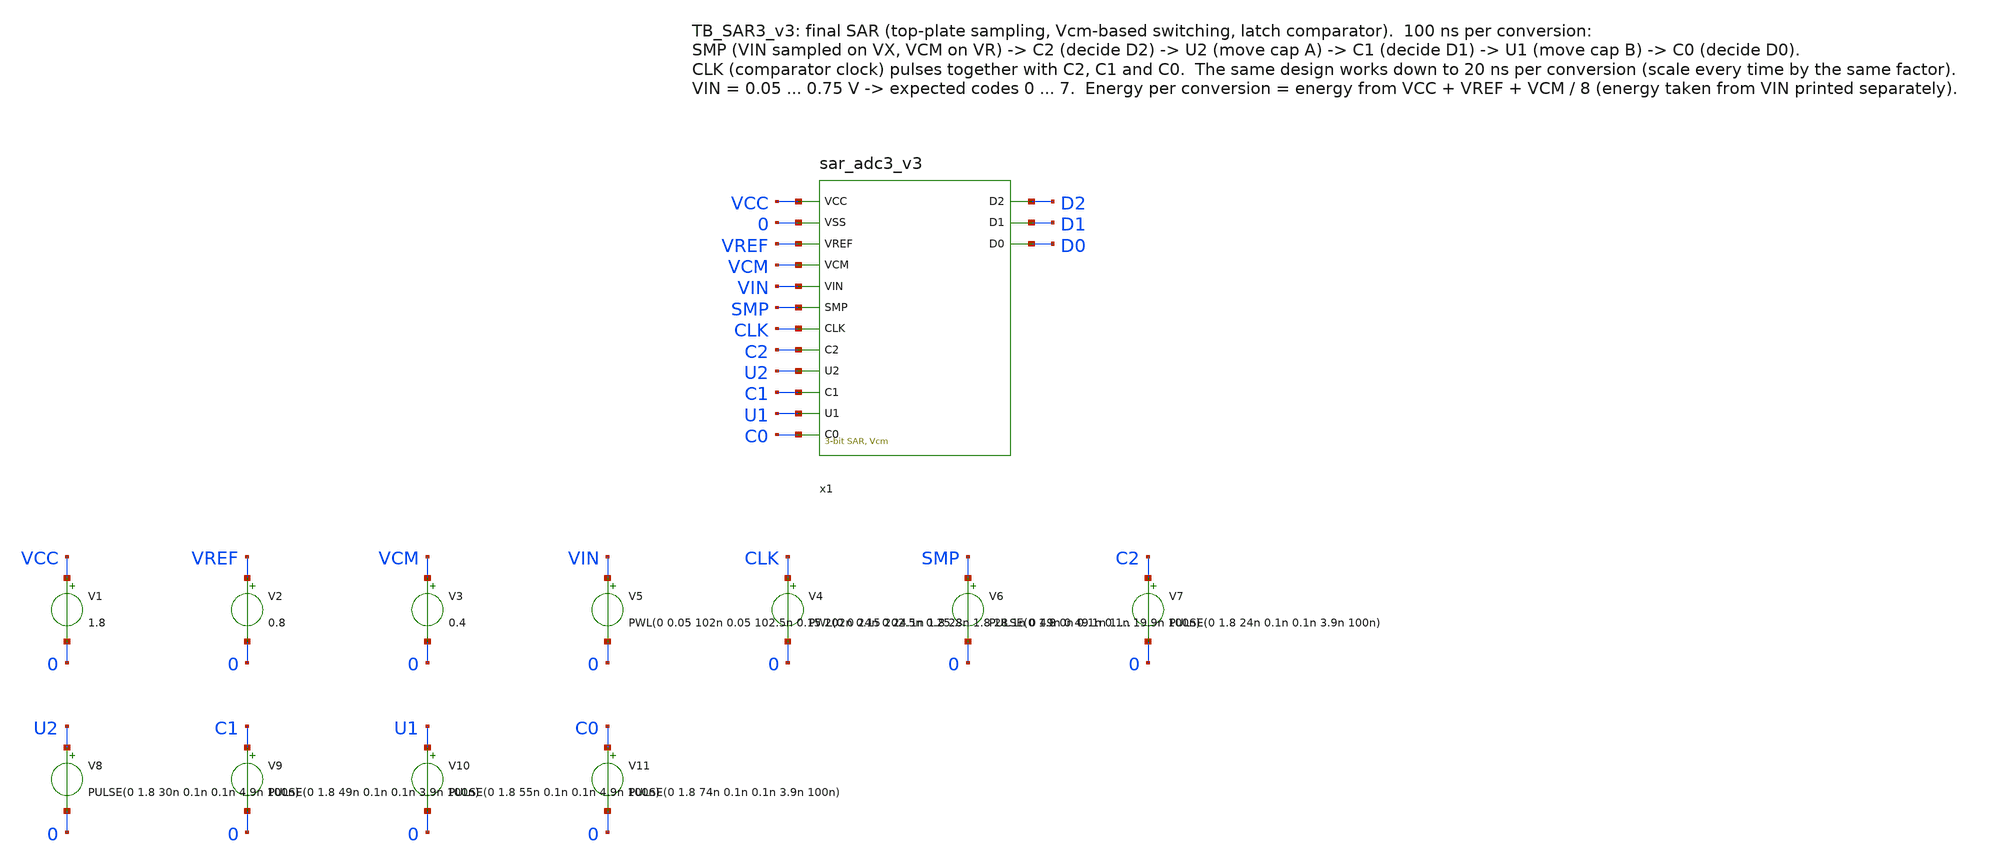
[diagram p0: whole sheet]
** sch_path: SAR_improved/TB_SAR3_v3.sch
**.subckt TB_SAR3_v3
x1 VCC 0 VREF VCM VIN SMP CLK C2 U2 C1 U1 C0 D2 D1 D0 sar_adc3_v3
V1 VCC 0 1.8
V2 VREF 0 0.8
V3 VCM 0 0.4
V5 VIN 0 PWL(0 0.05 102n 0.05 102.5n 0.15 202n 0.15 202.5n 0.25 302n 0.25 302.5n 0.35 402n 0.35
+ 402.5n 0.45 502n 0.45 502.5n 0.55 602n 0.55 602.5n 0.65 702n 0.65 702.5n 0.75)
V4 CLK 0 PWL(0 0 24n 0 24.1n 1.8 28n 1.8 28.1n 0 49n 0 49.1n 1.8 53n 1.8 53.1n 0 74n 0 74.1n 1.8 78n
+ 1.8 78.1n 0 100n 0) r=0
V6 SMP 0 PULSE(0 1.8 0n 0.1n 0.1n 19.9n 100n)
V7 C2 0 PULSE(0 1.8 24n 0.1n 0.1n 3.9n 100n)
V8 U2 0 PULSE(0 1.8 30n 0.1n 0.1n 4.9n 100n)
V9 C1 0 PULSE(0 1.8 49n 0.1n 0.1n 3.9n 100n)
V10 U1 0 PULSE(0 1.8 55n 0.1n 0.1n 4.9n 100n)
V11 C0 0 PULSE(0 1.8 74n 0.1n 0.1n 3.9n 100n)
**** begin user architecture code

.lib /home/ttuser/pdk/sky130A/libs.tech/combined/sky130.lib.spice tt
.option method=gear reltol=1e-4
.control
save all
tran 0.025n 800n
let code = 4*ceil((v(D2)-0.9)/10) + 2*ceil((v(D1)-0.9)/10) + ceil((v(D0)-0.9)/10)
meas tran code1 find code at=90n
meas tran code2 find code at=190n
meas tran code3 find code at=290n
meas tran code4 find code at=390n
meas tran code5 find code at=490n
meas tran code6 find code at=590n
meas tran code7 find code at=690n
meas tran code8 find code at=790n
let ptot = 1.8*(-i(V1)) + 0.8*(-i(V2)) + 0.4*(-i(V3))
let pin = v(VIN)*(-i(V5))
meas tran etot integ ptot from=0 to=800n
meas tran ein integ pin from=0 to=800n
let e_conv_pJ = etot/8*1e12
let e_from_vin_pJ = ein/8*1e12
let p_uW = etot/800e-9*1e6
print e_conv_pJ p_uW e_from_vin_pJ
plot v(VIN) v(x1.VX) v(x1.VR)
plot v(SMP) v(CLK)+2 v(x1.COM)+4
plot v(x1.x2.BPA) v(x1.x2.BPB)
plot v(D2) v(D1)+2 v(D0)+4
plot code v(VIN)
.endc

**** end user architecture code
**.ends
.end
